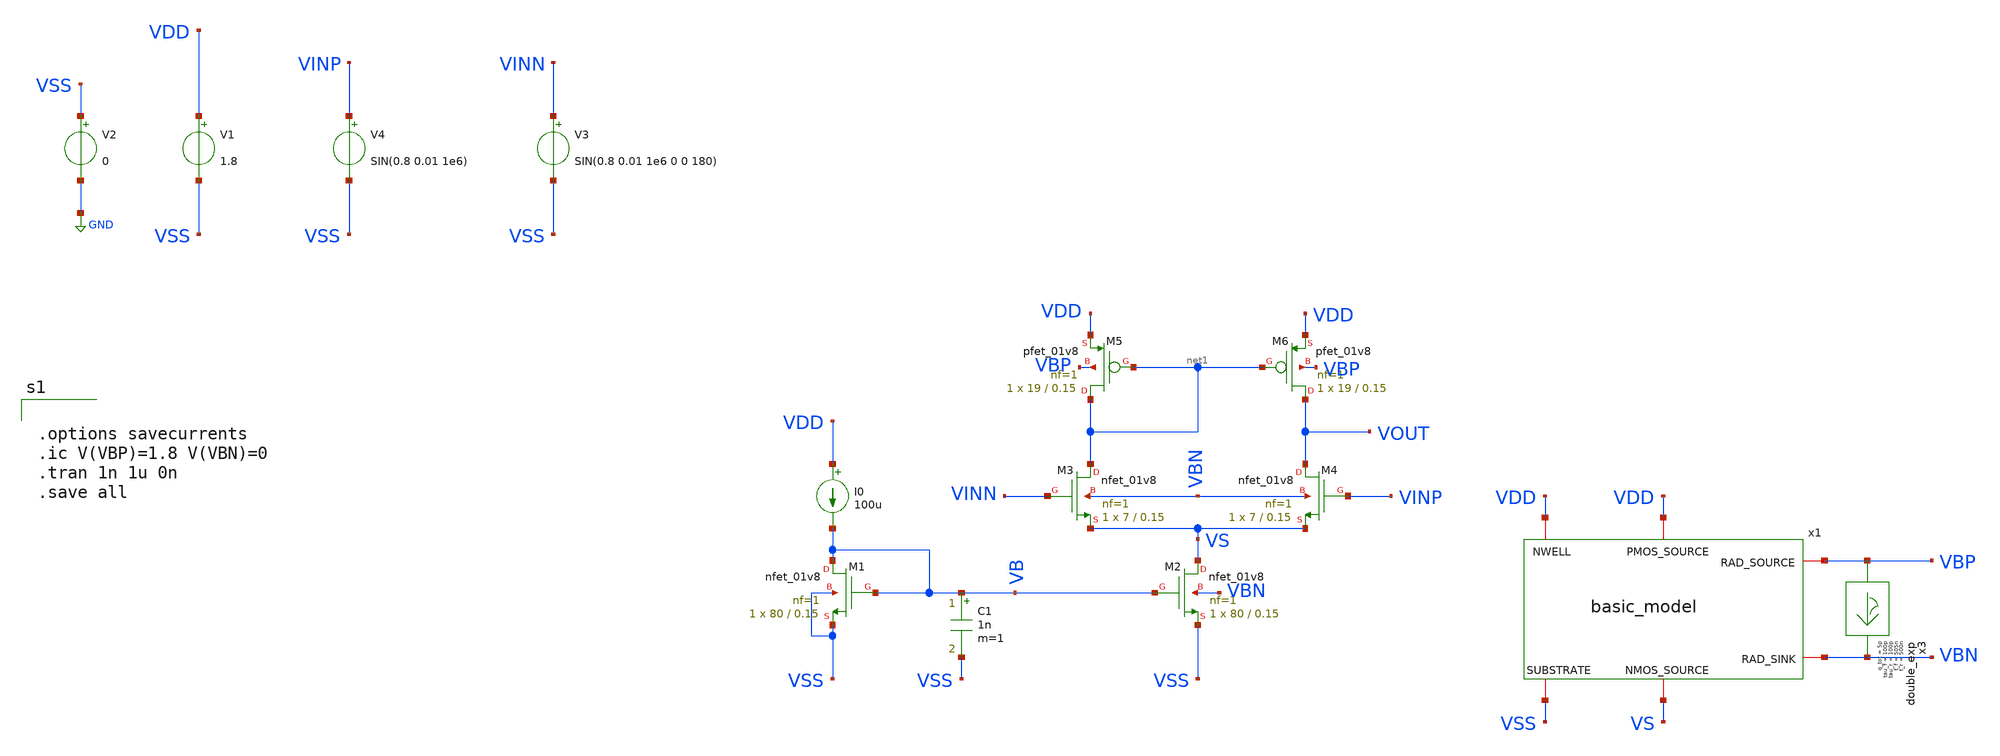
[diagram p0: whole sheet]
** sch_path: untitled-6.sch
**.subckt untitled-6
XM2 VS VB VSS VBN sky130_fd_pr__nfet_01v8 L=0.15 W=80 nf=1 ad='int((nf+1)/2) * W/nf * 0.29' as='int((nf+2)/2) * W/nf * 0.29'
+ pd='2*int((nf+1)/2) * (W/nf + 0.29)' ps='2*int((nf+2)/2) * (W/nf + 0.29)' nrd='0.29 / W' nrs='0.29 / W'
+ sa=0 sb=0 sd=0 mult=1 m=1
V1 VDD VSS 1.8
V2 VSS GND 0
XM1 VB VB VSS VSS sky130_fd_pr__nfet_01v8 L=0.15 W=80 nf=1 ad='int((nf+1)/2) * W/nf * 0.29' as='int((nf+2)/2) * W/nf * 0.29'
+ pd='2*int((nf+1)/2) * (W/nf + 0.29)' ps='2*int((nf+2)/2) * (W/nf + 0.29)' nrd='0.29 / W' nrs='0.29 / W'
+ sa=0 sb=0 sd=0 mult=1 m=1
I0 VDD VB 100u
XM3 net1 VINN VS VBN sky130_fd_pr__nfet_01v8 L=0.15 W=7 nf=1 ad='int((nf+1)/2) * W/nf * 0.29' as='int((nf+2)/2) * W/nf * 0.29'
+ pd='2*int((nf+1)/2) * (W/nf + 0.29)' ps='2*int((nf+2)/2) * (W/nf + 0.29)' nrd='0.29 / W' nrs='0.29 / W'
+ sa=0 sb=0 sd=0 mult=1 m=1
XM4 VOUT VINP VS VBN sky130_fd_pr__nfet_01v8 L=0.15 W=7 nf=1 ad='int((nf+1)/2) * W/nf * 0.29' as='int((nf+2)/2) * W/nf * 0.29'
+ pd='2*int((nf+1)/2) * (W/nf + 0.29)' ps='2*int((nf+2)/2) * (W/nf + 0.29)' nrd='0.29 / W' nrs='0.29 / W'
+ sa=0 sb=0 sd=0 mult=1 m=1
XM5 net1 net1 VDD VBP sky130_fd_pr__pfet_01v8 L=0.15 W=19 nf=1 ad='int((nf+1)/2) * W/nf * 0.29' as='int((nf+2)/2) * W/nf * 0.29'
+ pd='2*int((nf+1)/2) * (W/nf + 0.29)' ps='2*int((nf+2)/2) * (W/nf + 0.29)' nrd='0.29 / W' nrs='0.29 / W'
+ sa=0 sb=0 sd=0 mult=1 m=1
XM6 VOUT net1 VDD VBP sky130_fd_pr__pfet_01v8 L=0.15 W=19 nf=1 ad='int((nf+1)/2) * W/nf * 0.29' as='int((nf+2)/2) * W/nf * 0.29'
+ pd='2*int((nf+1)/2) * (W/nf + 0.29)' ps='2*int((nf+2)/2) * (W/nf + 0.29)' nrd='0.29 / W' nrs='0.29 / W'
+ sa=0 sb=0 sd=0 mult=1 m=1
V4 VINP VSS SIN(0.8 0.01 1e6)
V3 VINN VSS SIN(0.8 0.01 1e6 0 0 180)
C1 VB VSS 1n m=1
x3 VBP VBN double_exp t_r=500n tau_r=100p t_f=505n tau_f=100p q_tot=5p
x1 VDD VDD VBP VBN VS VSS basic_model
**** begin user architecture code


.options savecurrents
.ic V(VBP)=1.8 V(VBN)=0
.tran 1n 1u 0n
.save all



** opencircuitdesign pdks install
.lib $::SKYWATER_MODELS/sky130.lib.spice tt




.include /usr/local/share/rad_modeling_blocks/rad_modeling_blocks.spice


**** end user architecture code
**.ends

* expanding   symbol:  double_exp.sym # of pins=2
** sym_path: xschem_rad_library/double_exp.sym
** sch_path: xschem_rad_library/double_exp.sch
.subckt double_exp in out  t_r=0 t_f=0 tau_r=0 tau_f=0 q_tot=0
*.opin OUT
*.ipin IN
I1 IN OUT EXP(0 {q_tot / (t_f-t_r+tau_f-tau_r)} {t_r} {tau_r} {t_f} {tau_f})
.ends


* expanding   symbol:  OSCRE/latchup/basic_model.sym # of pins=6
** sym_path: latchup/basic_model.sym
** sch_path: latchup/basic_model.sch
.subckt basic_model PMOS_SOURCE NWELL RAD_SOURCE RAD_SINK NMOS_SOURCE SUBSTRATE   IS_N=1e-18
+  BF_N=100  VAF_N=50  IKF_N=0.01  CJE_N=0.2p  CJC_N=0.1p  TF_N=0.2n  TR_N=2n  IS_P=1e-18  BF_P=100  VAF_P=50
+  IKF_P=0.01  CJE_P=0.3p  CJC_P=0.15p  TF_P=0.3n  TR_P=3n
*.iopin NWELL
*.iopin SUBSTRATE
*.iopin RAD_SOURCE
*.iopin RAD_SINK
*.iopin NMOS_SOURCE
*.iopin PMOS_SOURCE
Q1 RAD_SINK RAD_SOURCE PMOS_SOURCE pnp_cust area=1 m=1
Q2 RAD_SOURCE RAD_SINK NMOS_SOURCE npn_cust area=1 m=1
R3 RAD_SINK SUBSTRATE 1000 m=1
R4 NWELL RAD_SOURCE 1000 m=1
**** begin user architecture code


.model npn_cust npn (IS={IS_N} BF={BF_N} VAF={VAF_N} IKF={IKF_N} CJE={CJE_N} CJC={CJC_N} TF={TF_N} TR={TR_N})
.model pnp_cust pnp (IS={IS_P} BF={BF_P} VAF={VAF_P} IKF={IKF_P} CJE={CJE_P} CJC={CJC_N} TF={TF_N} TR={TR_P})


**** end user architecture code
.ends

.GLOBAL GND
.end
